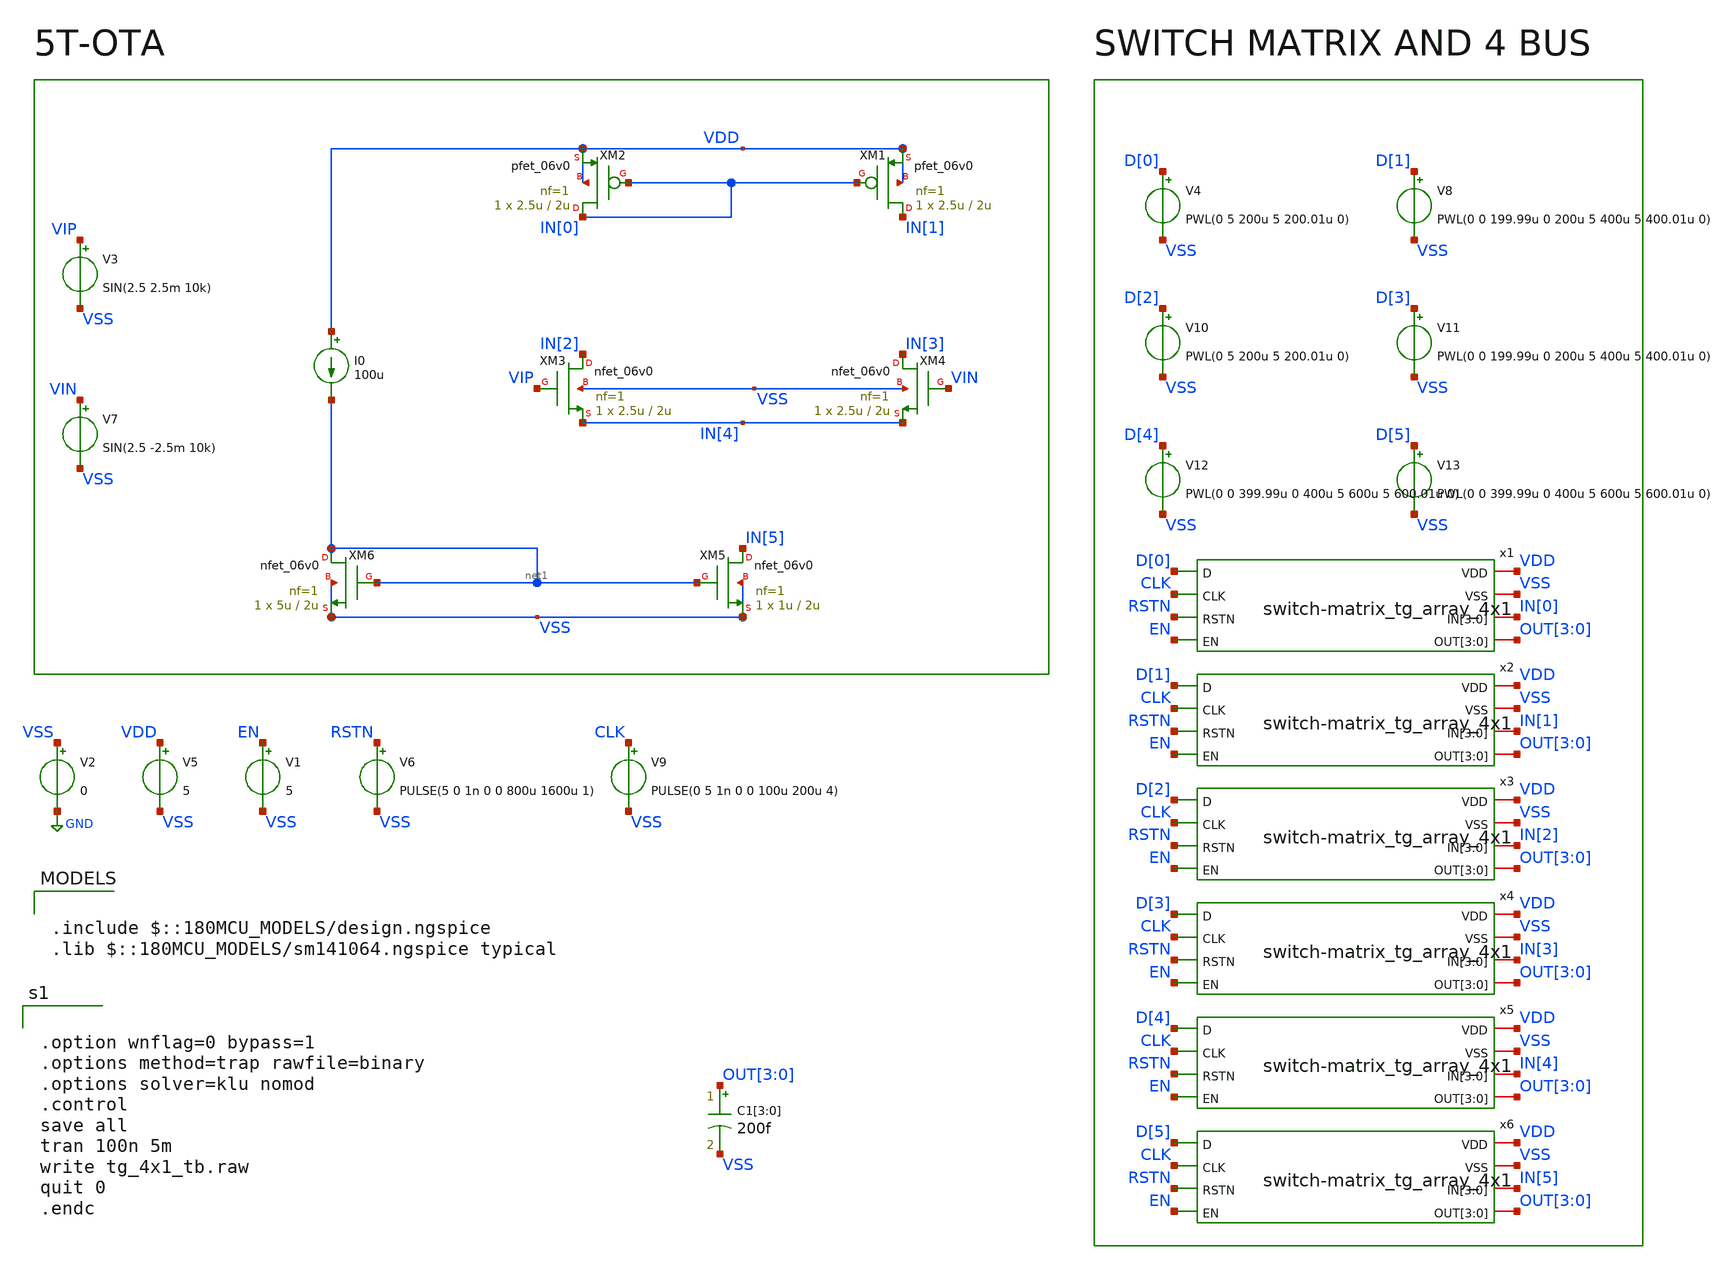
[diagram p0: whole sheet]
** sch_path: designs/libs/tb_analog/tb_switch-matrix/tb_switch-matrix_tg_array_4x1.sch
**.subckt tb_switch-matrix_tg_array_4x1
V2 VSS GND 0
V3 VIP VSS SIN(2.5 2.5m 10k)
V4 D[0] VSS PWL(0 5 200u 5 200.01u 0)
V5 VDD VSS 5
V9 CLK VSS PULSE(0 5 1n 0 0 100u 200u 4)
V1 EN VSS 5
V6 RSTN VSS PULSE(5 0 1n 0 0 800u 1600u 1)
XM1 IN[1] IN[0] VDD VDD pfet_06v0 L=2u W=2.5u nf=1 ad='int((nf+1)/2) * W/nf * 0.18u' as='int((nf+2)/2) * W/nf * 0.18u'
+ pd='2*int((nf+1)/2) * (W/nf + 0.18u)' ps='2*int((nf+2)/2) * (W/nf + 0.18u)' nrd='0.18u / W' nrs='0.18u / W'
+ sa=0 sb=0 sd=0 m=1
XM2 IN[0] IN[0] VDD VDD pfet_06v0 L=2u W=2.5u nf=1 ad='int((nf+1)/2) * W/nf * 0.18u' as='int((nf+2)/2) * W/nf * 0.18u'
+ pd='2*int((nf+1)/2) * (W/nf + 0.18u)' ps='2*int((nf+2)/2) * (W/nf + 0.18u)' nrd='0.18u / W' nrs='0.18u / W'
+ sa=0 sb=0 sd=0 m=1
XM3 IN[2] VIP IN[4] VSS nfet_06v0 L=2u W=2.5u nf=1 ad='int((nf+1)/2) * W/nf * 0.18u' as='int((nf+2)/2) * W/nf * 0.18u'
+ pd='2*int((nf+1)/2) * (W/nf + 0.18u)' ps='2*int((nf+2)/2) * (W/nf + 0.18u)' nrd='0.18u / W' nrs='0.18u / W'
+ sa=0 sb=0 sd=0 m=1
XM4 IN[3] VIN IN[4] VSS nfet_06v0 L=2u W=2.5u nf=1 ad='int((nf+1)/2) * W/nf * 0.18u' as='int((nf+2)/2) * W/nf * 0.18u'
+ pd='2*int((nf+1)/2) * (W/nf + 0.18u)' ps='2*int((nf+2)/2) * (W/nf + 0.18u)' nrd='0.18u / W' nrs='0.18u / W'
+ sa=0 sb=0 sd=0 m=1
XM5 IN[5] net1 VSS VSS nfet_06v0 L=2u W=1u nf=1 ad='int((nf+1)/2) * W/nf * 0.18u' as='int((nf+2)/2) * W/nf * 0.18u'
+ pd='2*int((nf+1)/2) * (W/nf + 0.18u)' ps='2*int((nf+2)/2) * (W/nf + 0.18u)' nrd='0.18u / W' nrs='0.18u / W'
+ sa=0 sb=0 sd=0 m=1
XM6 net1 net1 VSS VSS nfet_06v0 L=2u W=5u nf=1 ad='int((nf+1)/2) * W/nf * 0.18u' as='int((nf+2)/2) * W/nf * 0.18u'
+ pd='2*int((nf+1)/2) * (W/nf + 0.18u)' ps='2*int((nf+2)/2) * (W/nf + 0.18u)' nrd='0.18u / W' nrs='0.18u / W'
+ sa=0 sb=0 sd=0 m=1
I0 VDD net1 100u
V7 VIN VSS SIN(2.5 -2.5m 10k)
V8 D[1] VSS PWL(0 0 199.99u 0 200u 5 400u 5 400.01u 0)
V10 D[2] VSS PWL(0 5 200u 5 200.01u 0)
V11 D[3] VSS PWL(0 0 199.99u 0 200u 5 400u 5 400.01u 0)
V12 D[4] VSS PWL(0 0 399.99u 0 400u 5 600u 5 600.01u 0)
V13 D[5] VSS PWL(0 0 399.99u 0 400u 5 600u 5 600.01u 0)
C1[3] OUT[3] VSS 200f m=1
C1[2] OUT[2] VSS 200f m=1
C1[1] OUT[1] VSS 200f m=1
C1[0] OUT[0] VSS 200f m=1
x1 VDD VSS IN[0] IN[0] IN[0] IN[0] OUT[3] OUT[2] OUT[1] OUT[0] D[0] CLK RSTN EN
+ switch-matrix_tg_array_4x1
x2 VDD VSS IN[1] IN[1] IN[1] IN[1] OUT[3] OUT[2] OUT[1] OUT[0] D[1] CLK RSTN EN
+ switch-matrix_tg_array_4x1
x3 VDD VSS IN[2] IN[2] IN[2] IN[2] OUT[3] OUT[2] OUT[1] OUT[0] D[2] CLK RSTN EN
+ switch-matrix_tg_array_4x1
x4 VDD VSS IN[3] IN[3] IN[3] IN[3] OUT[3] OUT[2] OUT[1] OUT[0] D[3] CLK RSTN EN
+ switch-matrix_tg_array_4x1
x5 VDD VSS IN[4] IN[4] IN[4] IN[4] OUT[3] OUT[2] OUT[1] OUT[0] D[4] CLK RSTN EN
+ switch-matrix_tg_array_4x1
x6 VDD VSS IN[5] IN[5] IN[5] IN[5] OUT[3] OUT[2] OUT[1] OUT[0] D[5] CLK RSTN EN
+ switch-matrix_tg_array_4x1
**** begin user architecture code

.include $::180MCU_MODELS/design.ngspice
.lib $::180MCU_MODELS/sm141064.ngspice typical



.option wnflag=0 bypass=1
.options method=trap rawfile=binary
.options solver=klu nomod
.control
save all
tran 100n 5m
write tg_4x1_tb.raw
quit 0
.endc


**** end user architecture code
**.ends
.GLOBAL GND
.end
